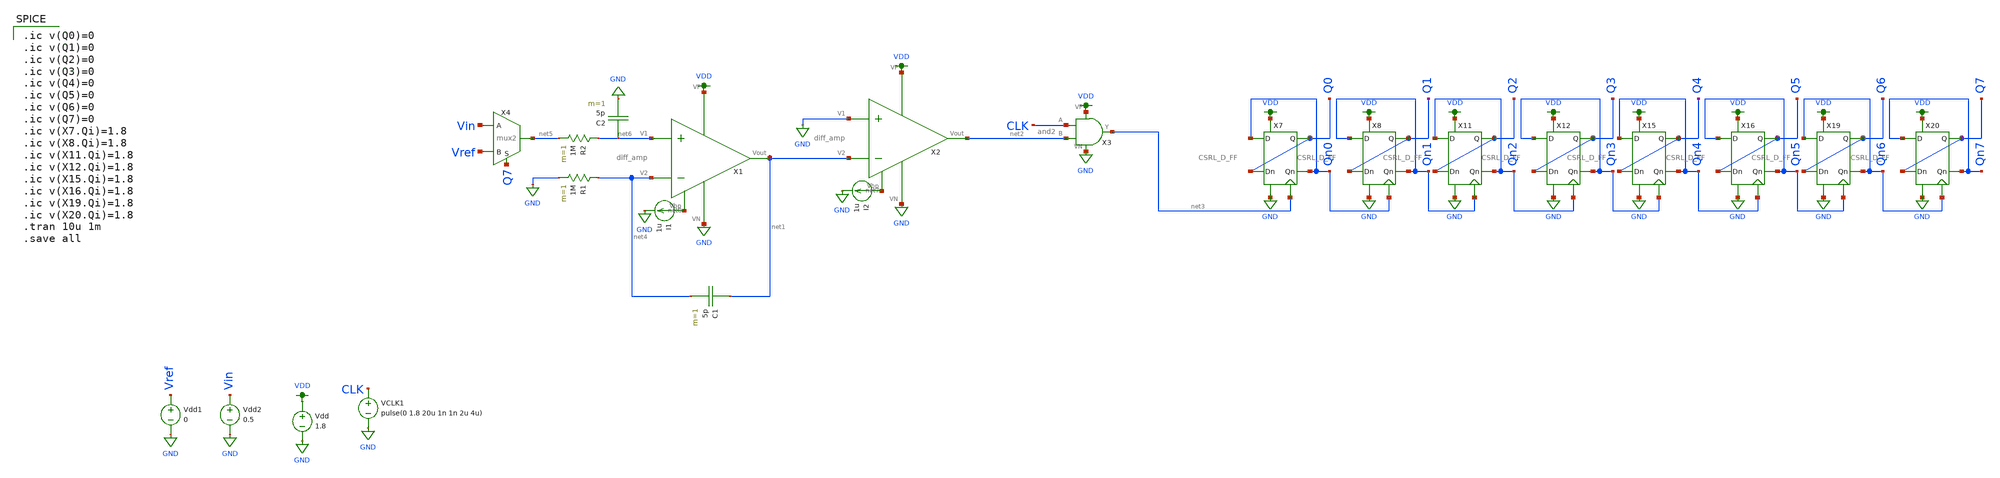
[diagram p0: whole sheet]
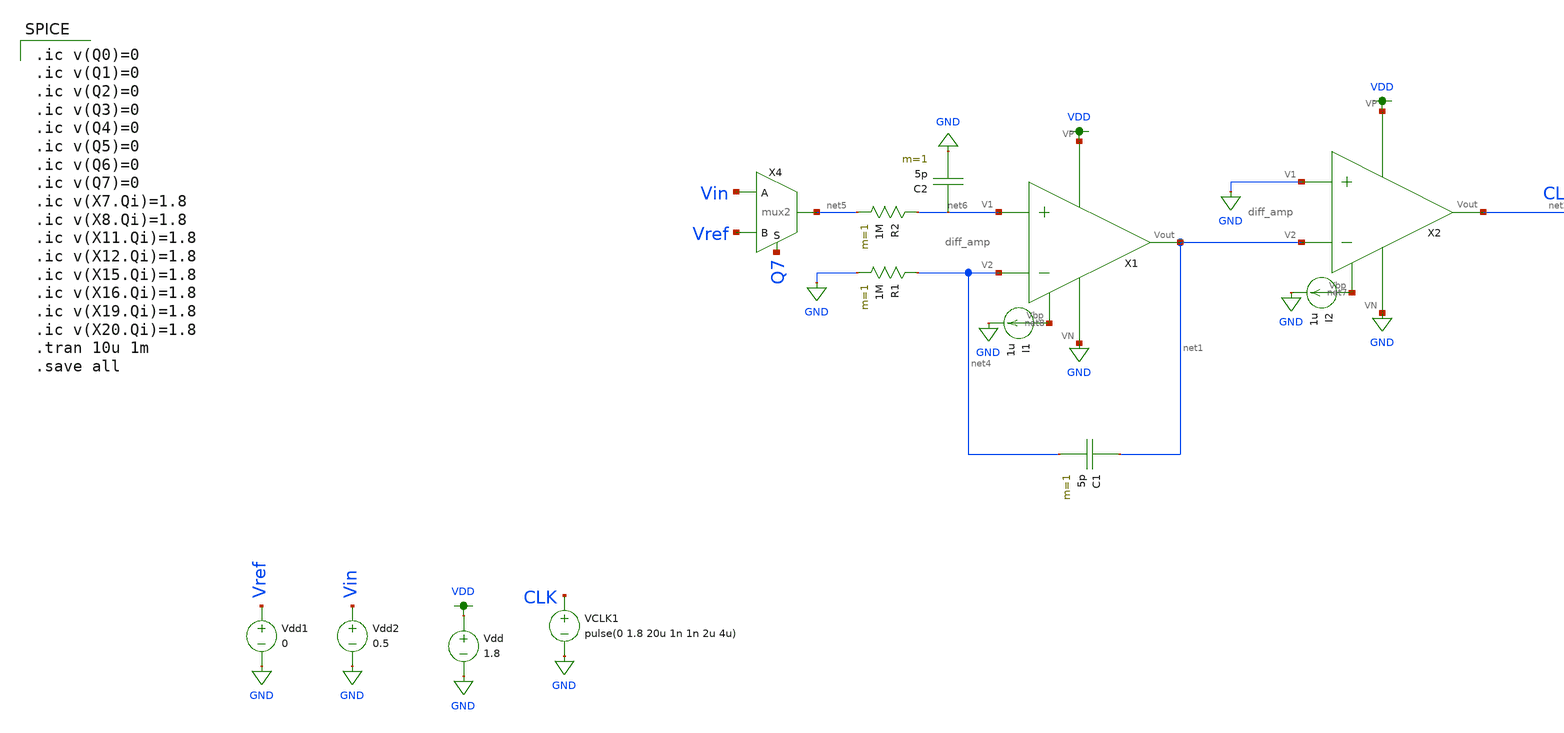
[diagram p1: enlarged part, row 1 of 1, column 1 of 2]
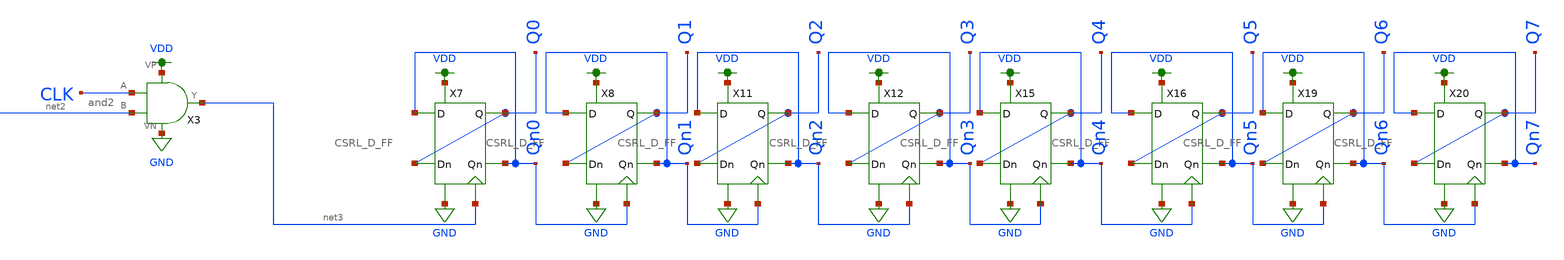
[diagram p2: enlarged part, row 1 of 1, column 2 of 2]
** sch_path: schematic/double-slope-sparsh.sch
**.subckt double-slope-sparsh
X2 VDD net7 net2 GND net1 GND diff_amp
X3 VDD CLK GND net3 net2 and2
Vdd VDD GND 1.8
Vdd1 Vref GND 0
Vdd2 Vin GND 0.5
X4 net5 Vin Vref Q7 mux2
X7 Q0 Qn0 Qn0 Q0 GND VDD net3 CSRL_D_FF
X8 Q1 Qn1 Qn1 Q1 GND VDD Qn0 CSRL_D_FF
X11 Q2 Qn2 Qn2 Q2 GND VDD Qn1 CSRL_D_FF
X12 Q3 Qn3 Qn3 Q3 GND VDD Qn2 CSRL_D_FF
X15 Q4 Qn4 Qn4 Q4 GND VDD Qn3 CSRL_D_FF
X16 Q5 Qn5 Qn5 Q5 GND VDD Qn4 CSRL_D_FF
X19 Q6 Qn6 Qn6 Q6 GND VDD Qn5 CSRL_D_FF
X20 Q7 Qn7 Qn7 Q7 GND VDD Qn6 CSRL_D_FF
I2 net7 GND 1u
C1 net1 net4 5p m=1
X1 VDD net8 net1 net6 net4 GND diff_amp
R1 net4 GND 1M m=1
C2 net6 GND 5p m=1
R2 net6 net5 1M m=1
I1 net8 GND 1u
VCLK1 CLK GND pulse(0 1.8 20u 1n 1n 2u 4u)
**** begin user architecture code

.option wnflag=1
.param MC_SWITCH=0.0
.lib ~/skywater/skywater-pdk/libraries/sky130_fd_pr_ngspice/latest/models/sky130.lib.spice tt


.ic v(Q0)=0
.ic v(Q1)=0
.ic v(Q2)=0
.ic v(Q3)=0
.ic v(Q4)=0
.ic v(Q5)=0
.ic v(Q6)=0
.ic v(Q7)=0
.ic v(X7.Qi)=1.8
.ic v(X8.Qi)=1.8
.ic v(X11.Qi)=1.8
.ic v(X12.Qi)=1.8
.ic v(X15.Qi)=1.8
.ic v(X16.Qi)=1.8
.ic v(X19.Qi)=1.8
.ic v(X20.Qi)=1.8
.tran 10u 1m
.save all

**** end user architecture code
**.ends
.GLOBAL GND
.GLOBAL VDD
.end
